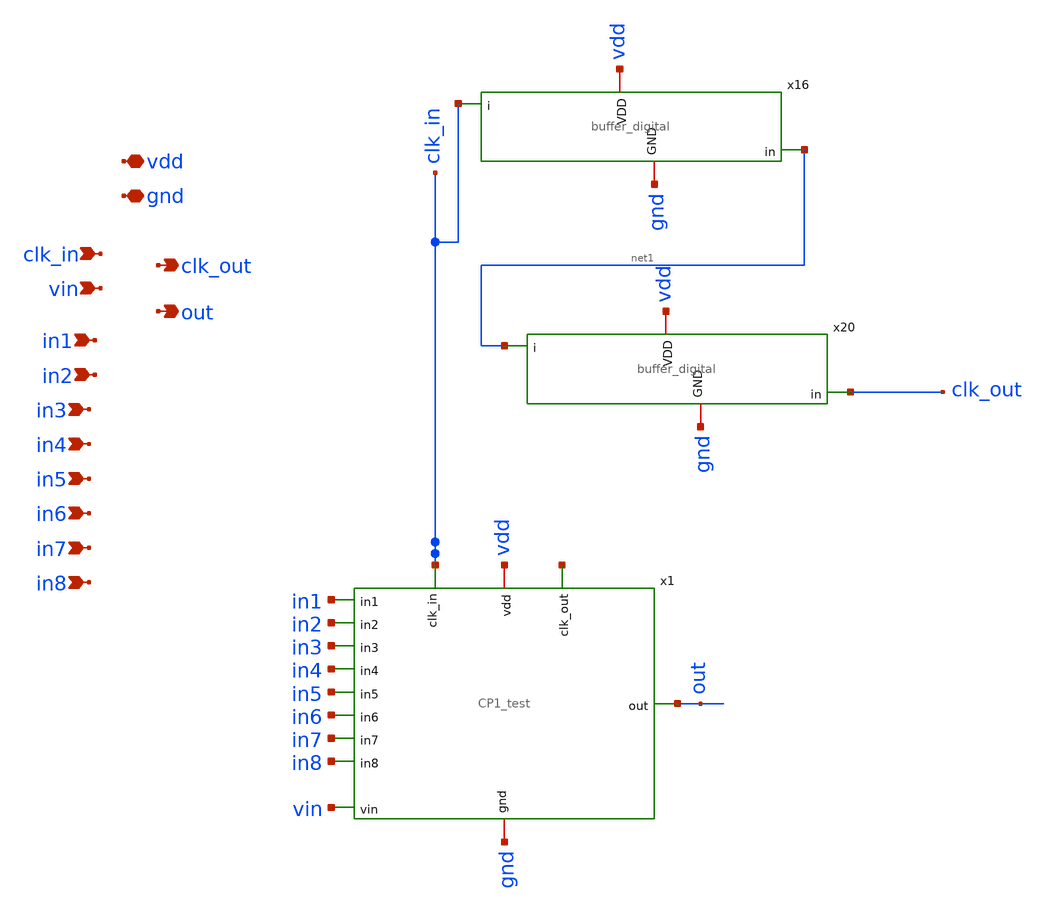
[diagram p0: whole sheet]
** sch_path: xschem/charge_pumps2/cp1_buffer_xschem.sch
**.subckt cp1_buffer_xschem clk_in gnd vdd out vin in1 in2 in3 in4 in5 in6 in7 in8 clk_out
*.ipin clk_in
*.iopin gnd
*.iopin vdd
*.opin out
*.ipin vin
*.ipin in1
*.ipin in2
*.ipin in3
*.ipin in4
*.ipin in5
*.ipin in6
*.ipin in7
*.ipin in8
*.opin clk_out
x1 gnd clk_in vin out in1 in2 in3 in4 in5 in6 in7 in8 vdd net2 CP1_test
x16 gnd vdd clk_in net1 buffer_digital
x20 gnd vdd net1 clk_out buffer_digital
**.ends
.end
